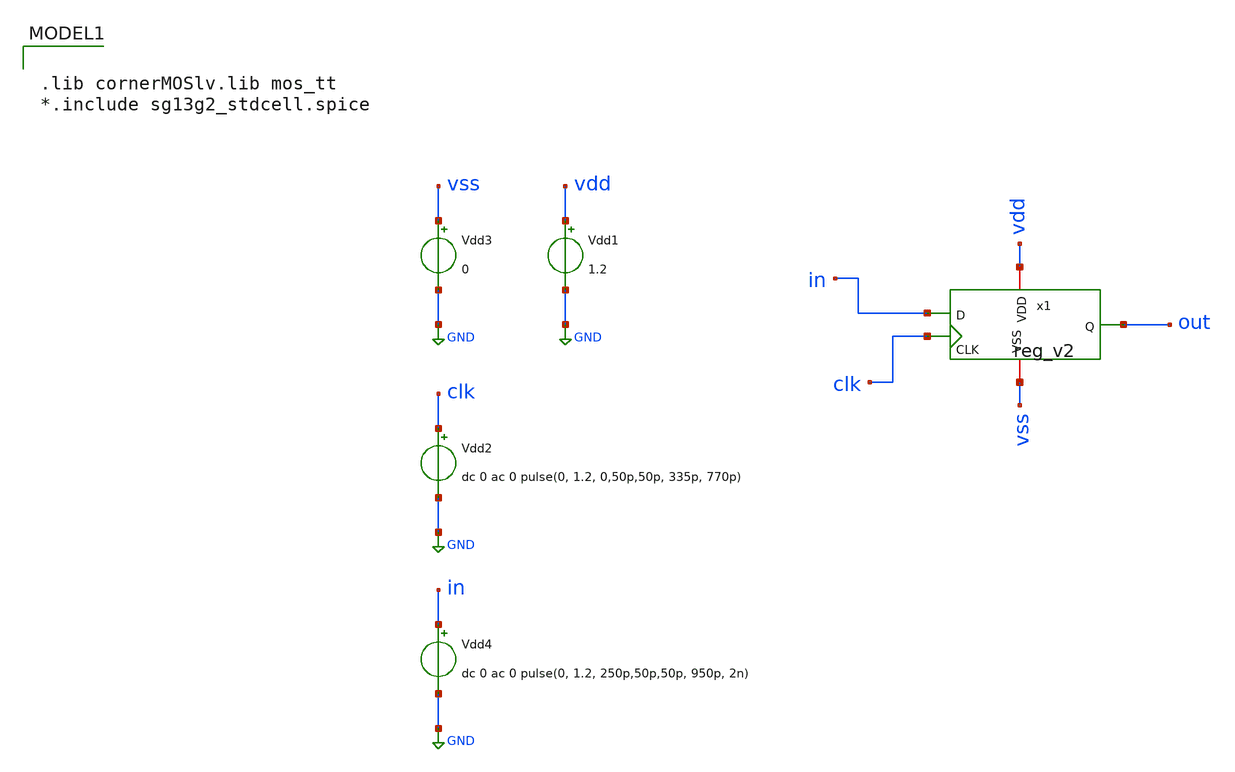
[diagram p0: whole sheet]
** sch_path: CDR4176-main/testbenches/tran/xschem/tb_reg.sch
**.subckt tb_reg
Vdd1 vdd GND 1.2
Vdd3 vss GND 0
Vdd2 clk GND dc 0 ac 0 pulse(0, 1.2, 0,50p,50p, 335p, 770p)
Vdd4 in GND dc 0 ac 0 pulse(0, 1.2, 250p,50p,50p, 950p, 2n)
x1 vdd clk vss out in reg_v2
**** begin user architecture code

.lib cornerMOSlv.lib mos_tt
*.include sg13g2_stdcell.spice




.save v(clk) v(in) v(out)


.tran 5p 6n

.control
run
set color0=white
write tran_logic.raw

.endc


**** end user architecture code
**.ends
.GLOBAL GND
.end
